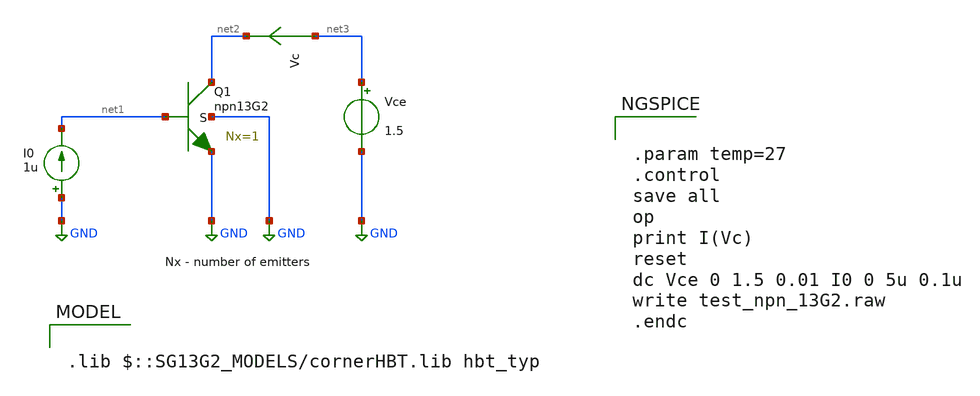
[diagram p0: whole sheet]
** sch_path: ihp-sg13g2/libs.tech/xschem/sg13g2_tests/dc_hbt_13g2.sch
* Copyright 2023 IHP PDK Authors
**.subckt dc_hbt_13g2
Vce net3 GND 1.5
I0 GND net1 1u
Vc net3 net2 0
.save i(vc)
XQ1 net2 net1 GND GND npn13G2 Nx=1 mm_ok=1
**** begin user architecture code

.lib $::SG13G2_MODELS/cornerHBT.lib hbt_typ



.param temp=27
.control
save all
op
print I(Vc)
reset
dc Vce 0 1.5 0.01 I0 0 5u 0.1u
write test_npn_13G2.raw
.endc


**** end user architecture code
**.ends
.GLOBAL GND
.end
